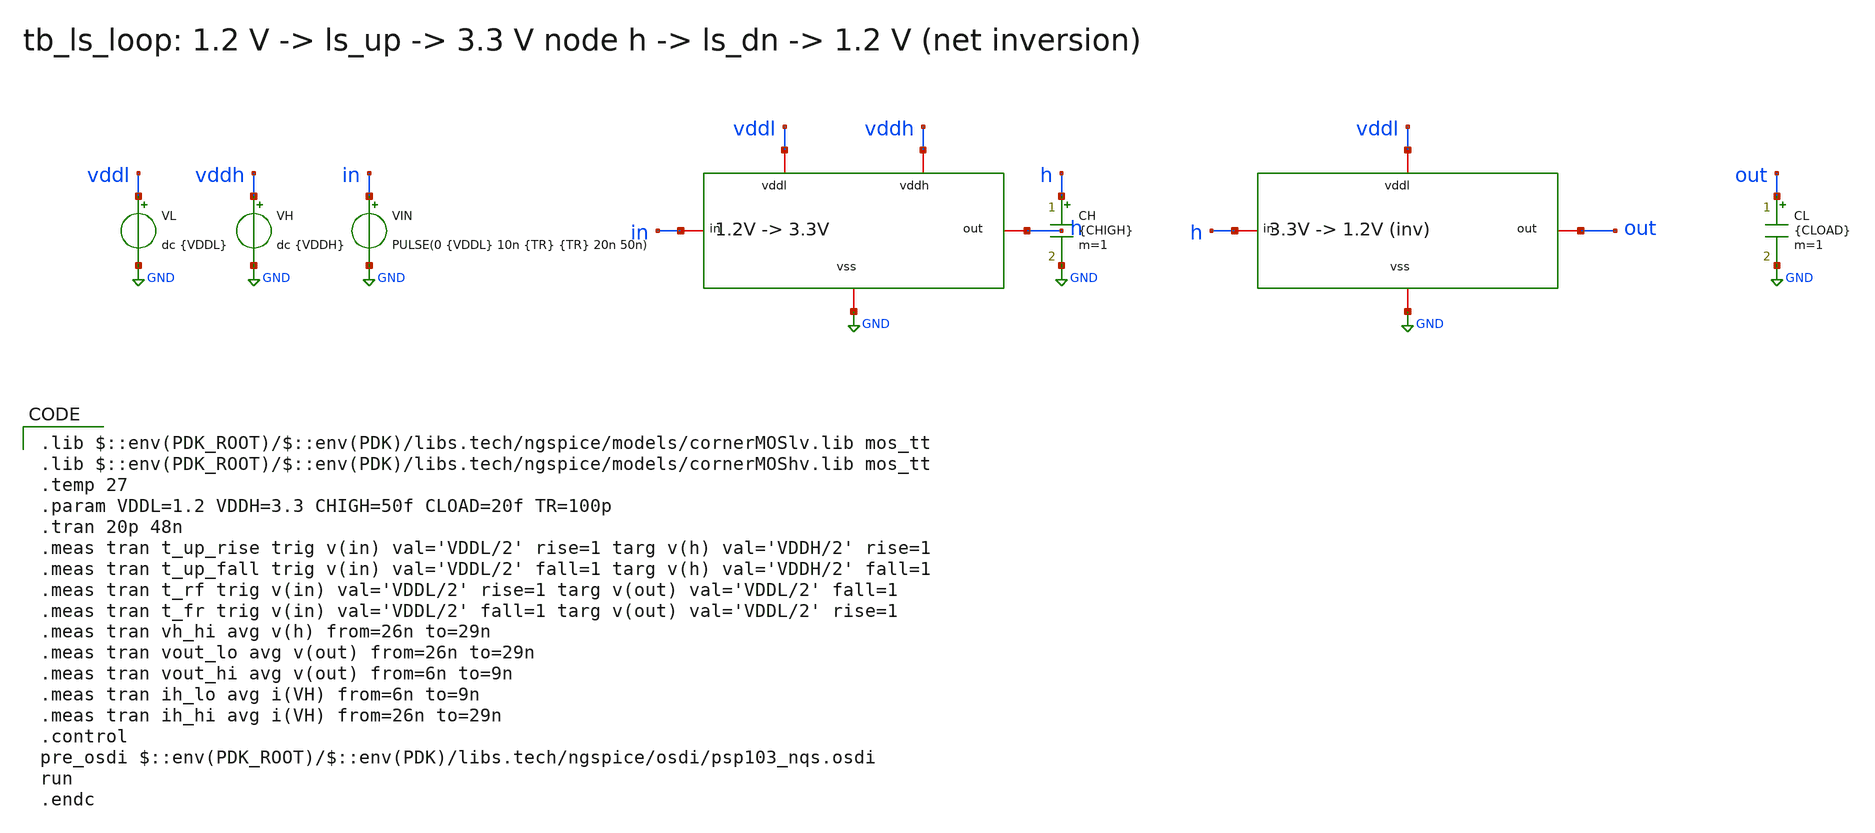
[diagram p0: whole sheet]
** sch_path: ls_pair/tb/tb_ls_loop.sch
**.subckt tb_ls_loop
x1 GND vddl vddh h in ls_up_1v2_3v3
x2 GND vddl out h ls_dn_3v3_1v2
VL vddl GND dc {VDDL}
VH vddh GND dc {VDDH}
VIN in GND PULSE(0 {VDDL} 10n {TR} {TR} 20n 50n)
CH h GND {CHIGH} m=1
CL out GND {CLOAD} m=1
**** begin user architecture code
 .lib $::env(PDK_ROOT)/$::env(PDK)/libs.tech/ngspice/models/cornerMOSlv.lib mos_tt
.lib $::env(PDK_ROOT)/$::env(PDK)/libs.tech/ngspice/models/cornerMOShv.lib mos_tt
.temp 27
.param VDDL=1.2 VDDH=3.3 CHIGH=50f CLOAD=20f TR=100p
.tran 20p 48n
.meas tran t_up_rise trig v(in) val='VDDL/2' rise=1 targ v(h) val='VDDH/2' rise=1
.meas tran t_up_fall trig v(in) val='VDDL/2' fall=1 targ v(h) val='VDDH/2' fall=1
.meas tran t_rf trig v(in) val='VDDL/2' rise=1 targ v(out) val='VDDL/2' fall=1
.meas tran t_fr trig v(in) val='VDDL/2' fall=1 targ v(out) val='VDDL/2' rise=1
.meas tran vh_hi avg v(h) from=26n to=29n
.meas tran vout_lo avg v(out) from=26n to=29n
.meas tran vout_hi avg v(out) from=6n to=9n
.meas tran ih_lo avg i(VH) from=6n to=9n
.meas tran ih_hi avg i(VH) from=26n to=29n
.control
pre_osdi $::env(PDK_ROOT)/$::env(PDK)/libs.tech/ngspice/osdi/psp103_nqs.osdi
run
.endc
**** end user architecture code
**.ends

* expanding   symbol:  ls_up_1v2_3v3.sym # of pins=5
** sym_path: ls_pair/xschem/ls_up_1v2_3v3.sym
** sch_path: ls_pair/xschem/ls_up_1v2_3v3.sch
.subckt ls_up_1v2_3v3 vss vddl vddh out in
*.iopin vss
*.iopin vddl
*.iopin vddh
*.opin out
*.ipin in
XM2 inb in vddl vddl sg13_lv_pmos w=1.2u l=0.13u ng=1 m=1 mm_ok=1
XM1 inb in vss vss sg13_lv_nmos w=0.6u l=0.13u ng=1 m=1 mm_ok=1
XM3 a in vss vss sg13_hv_nmos w=2u l=0.45u ng=1 m=4 mm_ok=1
XM6 a b vddh vddh sg13_hv_pmos w=2u l=0.4u ng=1 m=1 mm_ok=1
XM5 b a vddh vddh sg13_hv_pmos w=2u l=0.4u ng=1 m=1 mm_ok=1
XM4 b inb vss vss sg13_hv_nmos w=2u l=0.45u ng=1 m=4 mm_ok=1
XM16 out a vddh vddh sg13_hv_pmos w=2u l=0.4u ng=1 m=2 mm_ok=1
XM12 out a vss vss sg13_hv_nmos w=2u l=0.45u ng=1 m=1 mm_ok=1
.ends


* expanding   symbol:  ls_dn_3v3_1v2.sym # of pins=4
** sym_path: ls_pair/xschem/ls_dn_3v3_1v2.sym
** sch_path: ls_pair/xschem/ls_dn_3v3_1v2.sch
.subckt ls_dn_3v3_1v2 vss vddl out in
*.iopin vss
*.iopin vddl
*.opin out
*.ipin in
XMP1 out in vddl vddl sg13_hv_pmos w=1u l=0.45u ng=1 m=1 mm_ok=1
XMN1 out in vss vss sg13_hv_nmos w=0.8u l=0.45u ng=1 m=1 mm_ok=1
.ends

.GLOBAL GND
.end
